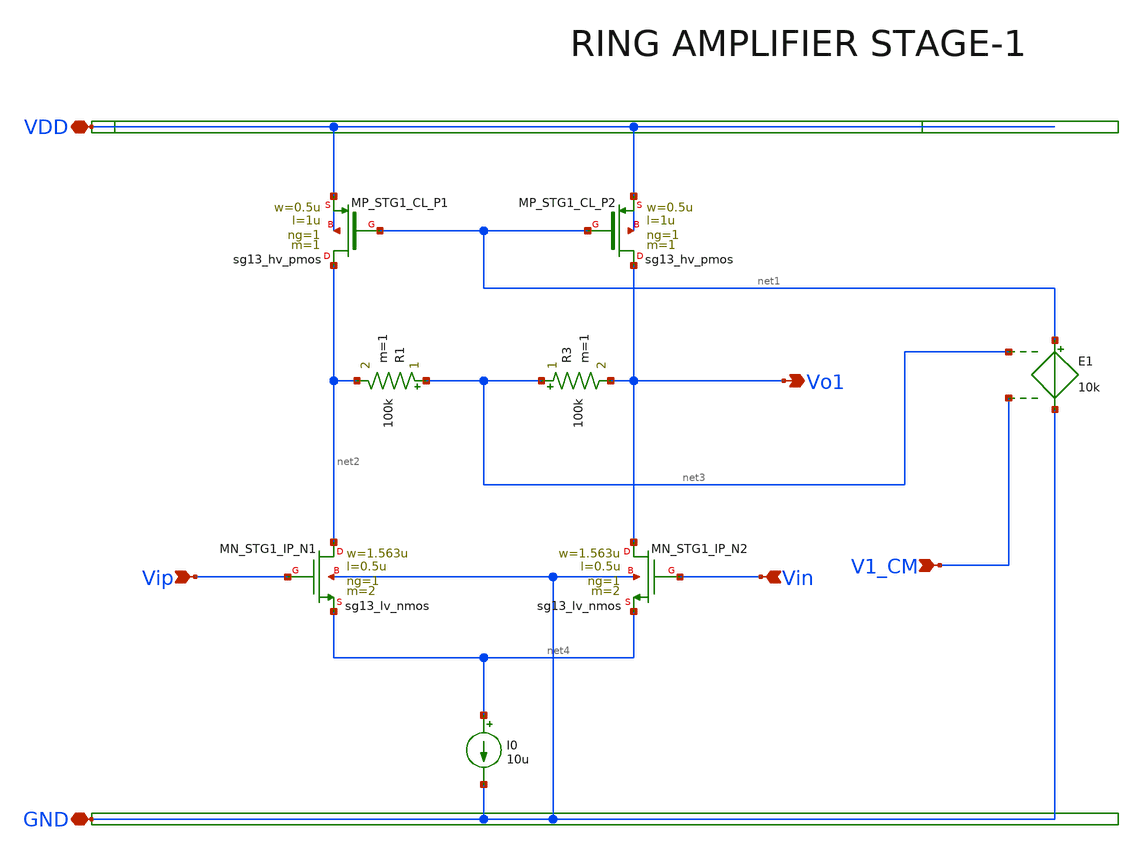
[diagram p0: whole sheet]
** sch_path: Design Files/RAMP/Fully-Diff-RAMP/STG1.sch
**.subckt STG1 VDD GND Vo1 Vip Vin V1_CM
*.iopin VDD
*.iopin GND
*.opin Vo1
*.ipin Vip
*.ipin Vin
*.ipin V1_CM
R1 net3 net2 100k m=1
R3 net3 Vo1 100k m=1
XMN_STG1_IP_N1 net2 Vip net4 GND sg13_lv_nmos w=1.563u l=0.5u ng=1 m=2 mm_ok=1
XMN_STG1_IP_N2 Vo1 Vin net4 GND sg13_lv_nmos w=1.563u l=0.5u ng=1 m=2 mm_ok=1
I0 net4 GND 10u
XMP_STG1_CL_P1 net2 net1 VDD VDD sg13_hv_pmos w=0.5u l=1u ng=1 m=1 mm_ok=1
XMP_STG1_CL_P2 Vo1 net1 VDD VDD sg13_hv_pmos w=0.5u l=1u ng=1 m=1 mm_ok=1
E1 net1 GND net3 V1_CM 10k
**.ends
.end
